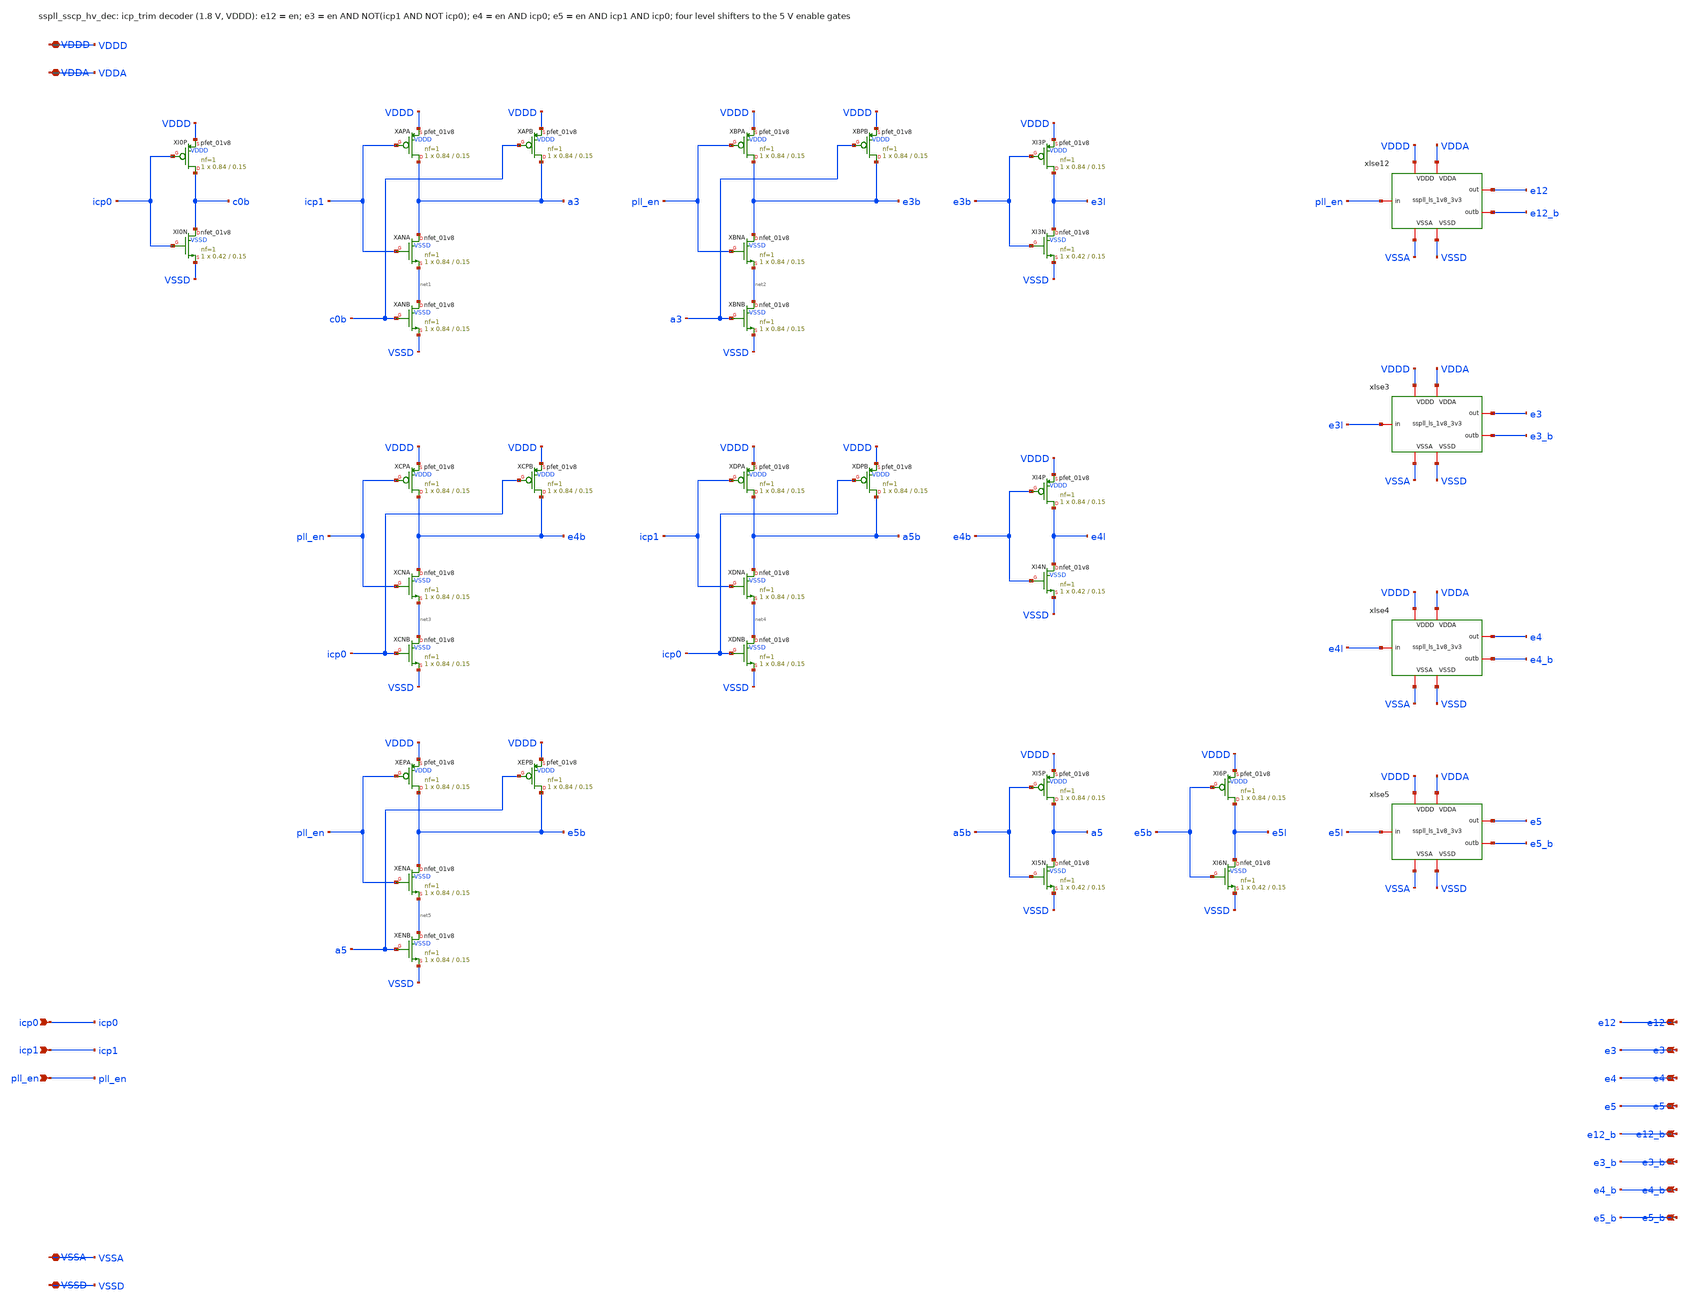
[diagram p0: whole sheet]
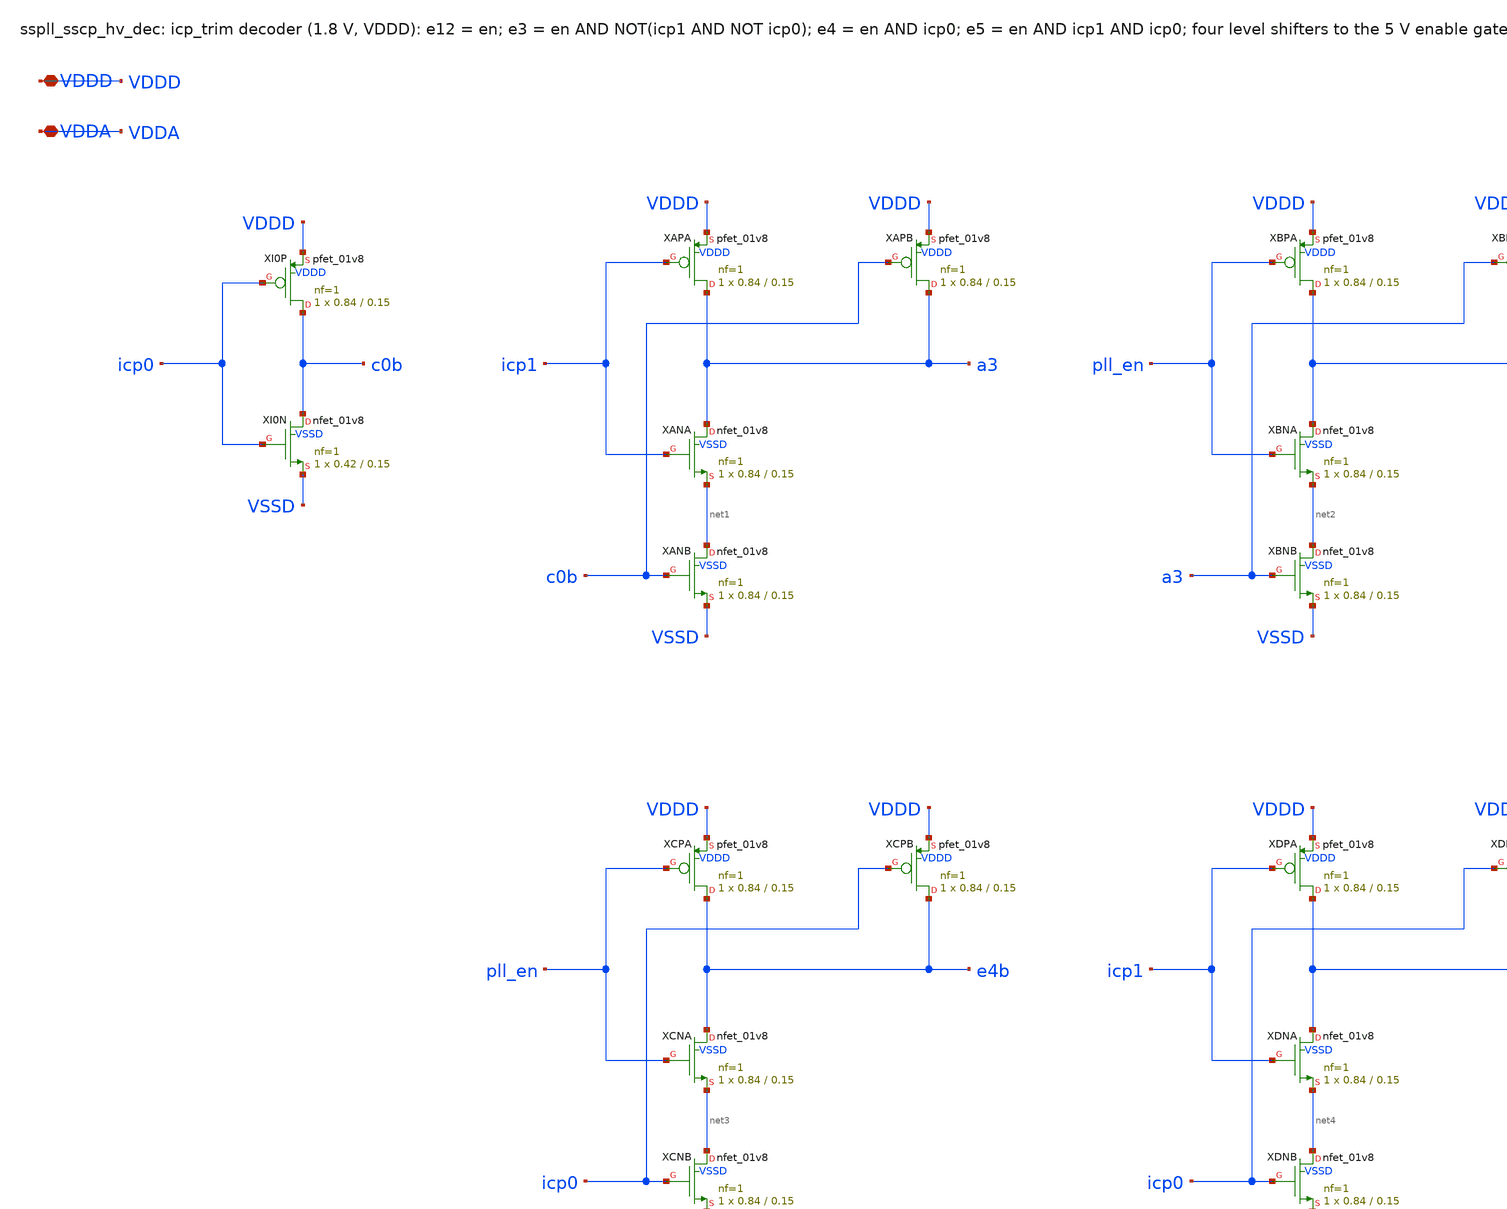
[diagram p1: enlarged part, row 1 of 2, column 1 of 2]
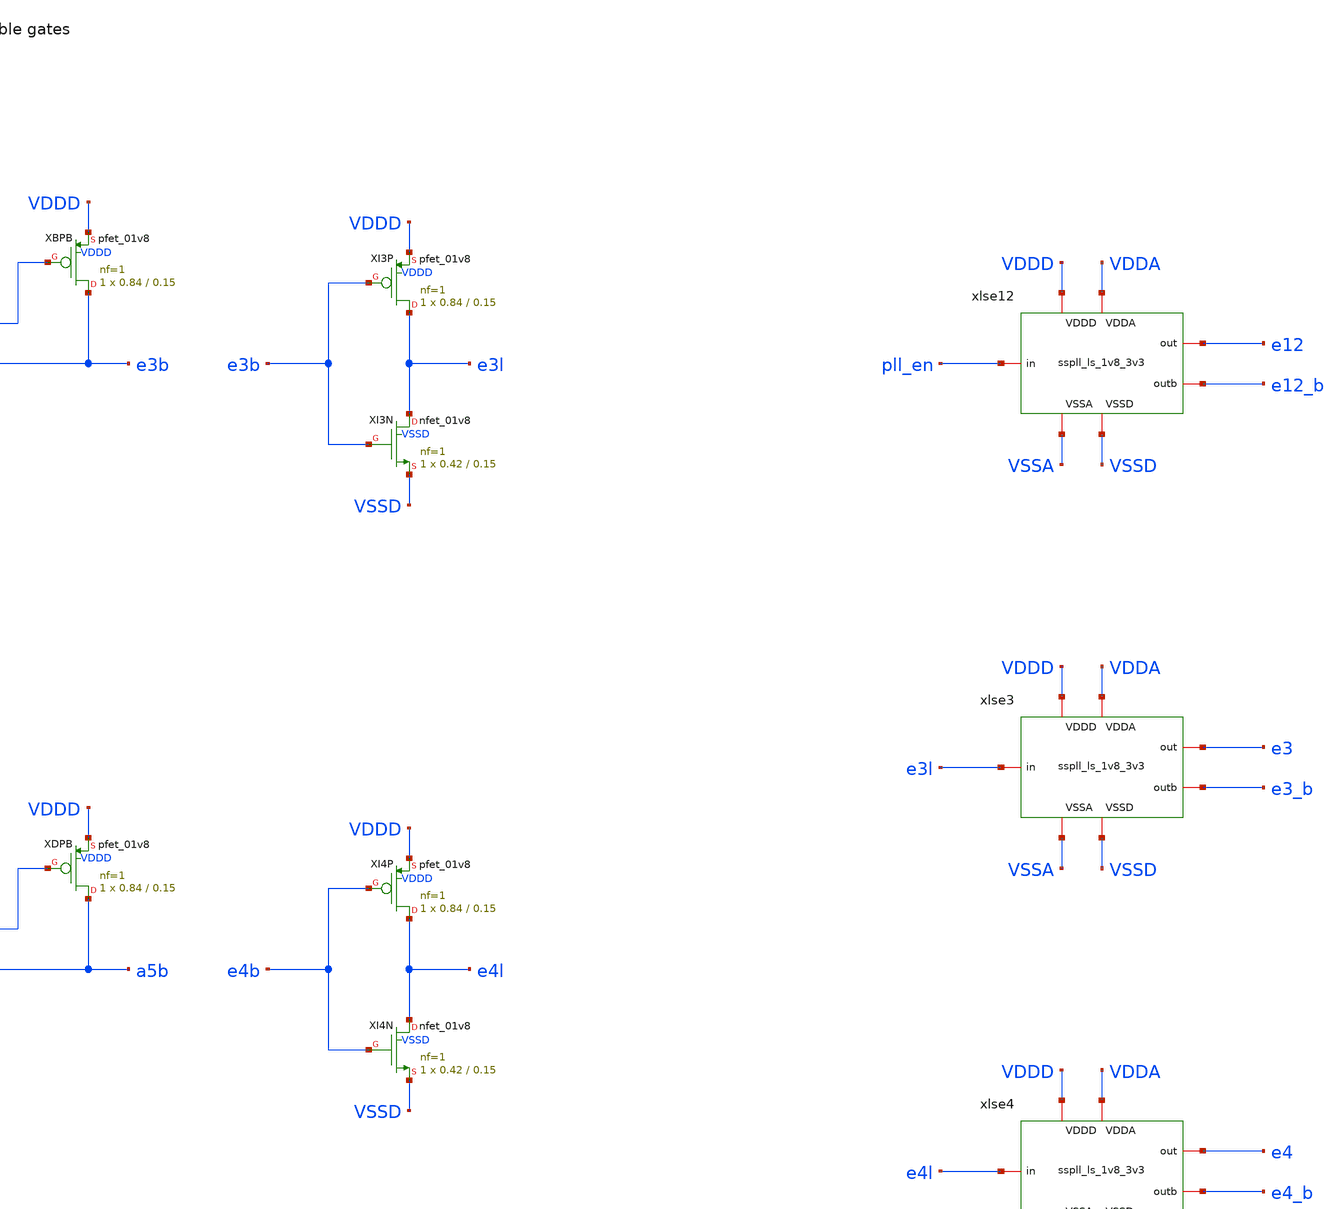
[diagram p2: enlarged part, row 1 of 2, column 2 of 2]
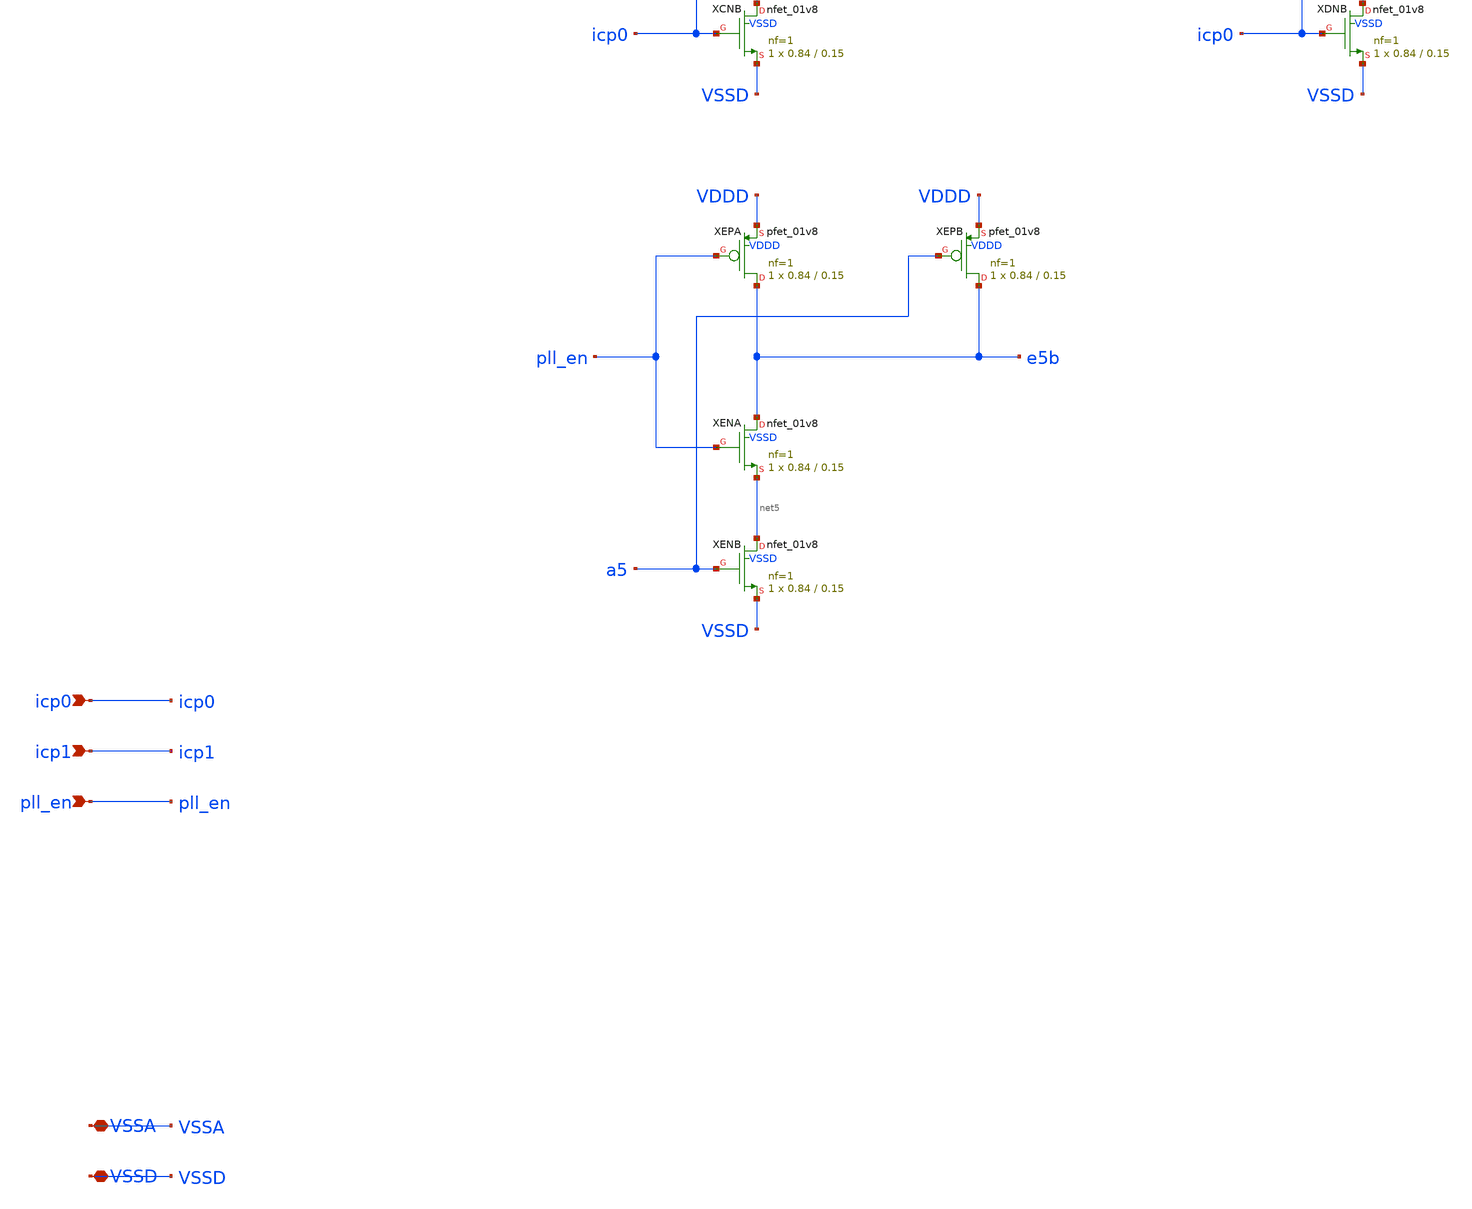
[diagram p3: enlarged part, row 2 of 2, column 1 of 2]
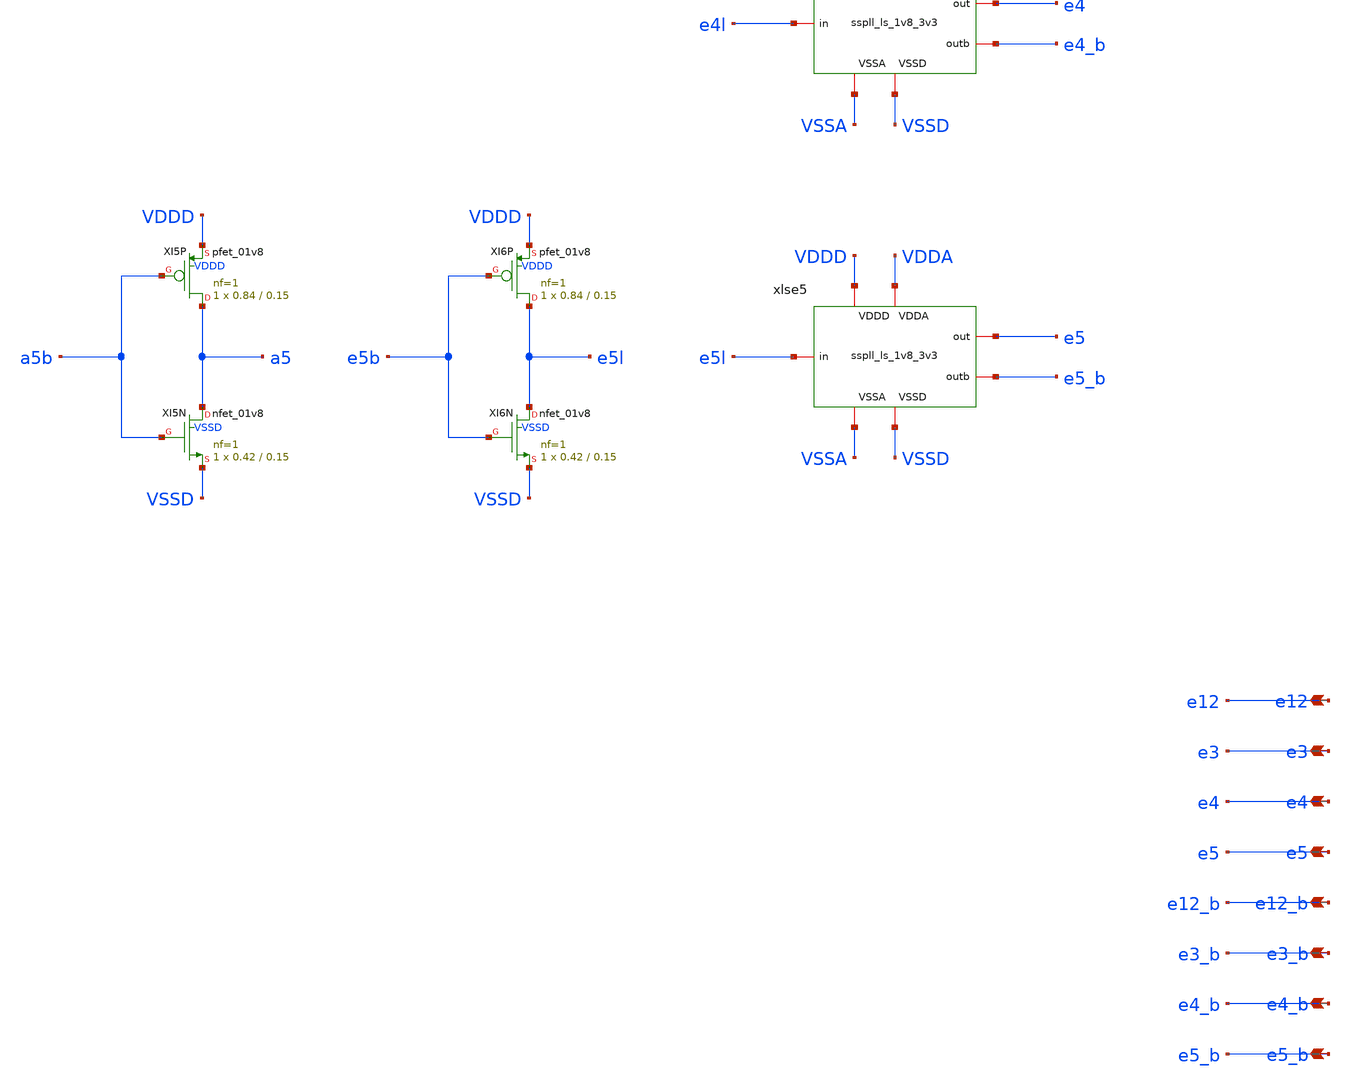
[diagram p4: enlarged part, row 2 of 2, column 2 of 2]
** sch_path: xschem/sscp_hv/sspll_sscp_hv_dec.sch
**.subckt sspll_sscp_hv_dec icp0 icp1 pll_en e12 e3 e4 e5 e12_b e3_b e4_b e5_b VDDD VDDA VSSA VSSD
*.ipin icp0
*.ipin icp1
*.ipin pll_en
*.opin e12
*.opin e3
*.opin e4
*.opin e5
*.opin e12_b
*.opin e3_b
*.opin e4_b
*.opin e5_b
*.iopin VDDD
*.iopin VDDA
*.iopin VSSA
*.iopin VSSD
XXI0P c0b icp0 VDDD VDDD sky130_fd_pr__pfet_01v8 L=0.15 W=0.84 nf=1 ad='int((nf+1)/2) * W/nf * 0.29'
+ as='int((nf+2)/2) * W/nf * 0.29' pd='2*int((nf+1)/2) * (W/nf + 0.29)' ps='2*int((nf+2)/2) * (W/nf + 0.29)'
+ nrd='0.29 / W' nrs='0.29 / W' sa=0 sb=0 sd=0 mult=1 m=1
XXI0N c0b icp0 VSSD VSSD sky130_fd_pr__nfet_01v8 L=0.15 W=0.42 nf=1 ad='int((nf+1)/2) * W/nf * 0.29'
+ as='int((nf+2)/2) * W/nf * 0.29' pd='2*int((nf+1)/2) * (W/nf + 0.29)' ps='2*int((nf+2)/2) * (W/nf + 0.29)'
+ nrd='0.29 / W' nrs='0.29 / W' sa=0 sb=0 sd=0 mult=1 m=1
XXAPA a3 icp1 VDDD VDDD sky130_fd_pr__pfet_01v8 L=0.15 W=0.84 nf=1 ad='int((nf+1)/2) * W/nf * 0.29' as='int((nf+2)/2) * W/nf * 0.29'
+ pd='2*int((nf+1)/2) * (W/nf + 0.29)' ps='2*int((nf+2)/2) * (W/nf + 0.29)' nrd='0.29 / W' nrs='0.29 / W'
+ sa=0 sb=0 sd=0 mult=1 m=1
XXAPB a3 c0b VDDD VDDD sky130_fd_pr__pfet_01v8 L=0.15 W=0.84 nf=1 ad='int((nf+1)/2) * W/nf * 0.29' as='int((nf+2)/2) * W/nf * 0.29'
+ pd='2*int((nf+1)/2) * (W/nf + 0.29)' ps='2*int((nf+2)/2) * (W/nf + 0.29)' nrd='0.29 / W' nrs='0.29 / W'
+ sa=0 sb=0 sd=0 mult=1 m=1
XXANA a3 icp1 net1 VSSD sky130_fd_pr__nfet_01v8 L=0.15 W=0.84 nf=1 ad='int((nf+1)/2) * W/nf * 0.29' as='int((nf+2)/2) * W/nf * 0.29'
+ pd='2*int((nf+1)/2) * (W/nf + 0.29)' ps='2*int((nf+2)/2) * (W/nf + 0.29)' nrd='0.29 / W' nrs='0.29 / W'
+ sa=0 sb=0 sd=0 mult=1 m=1
XXANB net1 c0b VSSD VSSD sky130_fd_pr__nfet_01v8 L=0.15 W=0.84 nf=1 ad='int((nf+1)/2) * W/nf * 0.29'
+ as='int((nf+2)/2) * W/nf * 0.29' pd='2*int((nf+1)/2) * (W/nf + 0.29)' ps='2*int((nf+2)/2) * (W/nf + 0.29)'
+ nrd='0.29 / W' nrs='0.29 / W' sa=0 sb=0 sd=0 mult=1 m=1
XXBPA e3b pll_en VDDD VDDD sky130_fd_pr__pfet_01v8 L=0.15 W=0.84 nf=1 ad='int((nf+1)/2) * W/nf * 0.29'
+ as='int((nf+2)/2) * W/nf * 0.29' pd='2*int((nf+1)/2) * (W/nf + 0.29)' ps='2*int((nf+2)/2) * (W/nf + 0.29)'
+ nrd='0.29 / W' nrs='0.29 / W' sa=0 sb=0 sd=0 mult=1 m=1
XXBPB e3b a3 VDDD VDDD sky130_fd_pr__pfet_01v8 L=0.15 W=0.84 nf=1 ad='int((nf+1)/2) * W/nf * 0.29' as='int((nf+2)/2) * W/nf * 0.29'
+ pd='2*int((nf+1)/2) * (W/nf + 0.29)' ps='2*int((nf+2)/2) * (W/nf + 0.29)' nrd='0.29 / W' nrs='0.29 / W'
+ sa=0 sb=0 sd=0 mult=1 m=1
XXBNA e3b pll_en net2 VSSD sky130_fd_pr__nfet_01v8 L=0.15 W=0.84 nf=1 ad='int((nf+1)/2) * W/nf * 0.29'
+ as='int((nf+2)/2) * W/nf * 0.29' pd='2*int((nf+1)/2) * (W/nf + 0.29)' ps='2*int((nf+2)/2) * (W/nf + 0.29)'
+ nrd='0.29 / W' nrs='0.29 / W' sa=0 sb=0 sd=0 mult=1 m=1
XXBNB net2 a3 VSSD VSSD sky130_fd_pr__nfet_01v8 L=0.15 W=0.84 nf=1 ad='int((nf+1)/2) * W/nf * 0.29' as='int((nf+2)/2) * W/nf * 0.29'
+ pd='2*int((nf+1)/2) * (W/nf + 0.29)' ps='2*int((nf+2)/2) * (W/nf + 0.29)' nrd='0.29 / W' nrs='0.29 / W'
+ sa=0 sb=0 sd=0 mult=1 m=1
XXCPA e4b pll_en VDDD VDDD sky130_fd_pr__pfet_01v8 L=0.15 W=0.84 nf=1 ad='int((nf+1)/2) * W/nf * 0.29'
+ as='int((nf+2)/2) * W/nf * 0.29' pd='2*int((nf+1)/2) * (W/nf + 0.29)' ps='2*int((nf+2)/2) * (W/nf + 0.29)'
+ nrd='0.29 / W' nrs='0.29 / W' sa=0 sb=0 sd=0 mult=1 m=1
XXCPB e4b icp0 VDDD VDDD sky130_fd_pr__pfet_01v8 L=0.15 W=0.84 nf=1 ad='int((nf+1)/2) * W/nf * 0.29'
+ as='int((nf+2)/2) * W/nf * 0.29' pd='2*int((nf+1)/2) * (W/nf + 0.29)' ps='2*int((nf+2)/2) * (W/nf + 0.29)'
+ nrd='0.29 / W' nrs='0.29 / W' sa=0 sb=0 sd=0 mult=1 m=1
XXCNA e4b pll_en net3 VSSD sky130_fd_pr__nfet_01v8 L=0.15 W=0.84 nf=1 ad='int((nf+1)/2) * W/nf * 0.29'
+ as='int((nf+2)/2) * W/nf * 0.29' pd='2*int((nf+1)/2) * (W/nf + 0.29)' ps='2*int((nf+2)/2) * (W/nf + 0.29)'
+ nrd='0.29 / W' nrs='0.29 / W' sa=0 sb=0 sd=0 mult=1 m=1
XXCNB net3 icp0 VSSD VSSD sky130_fd_pr__nfet_01v8 L=0.15 W=0.84 nf=1 ad='int((nf+1)/2) * W/nf * 0.29'
+ as='int((nf+2)/2) * W/nf * 0.29' pd='2*int((nf+1)/2) * (W/nf + 0.29)' ps='2*int((nf+2)/2) * (W/nf + 0.29)'
+ nrd='0.29 / W' nrs='0.29 / W' sa=0 sb=0 sd=0 mult=1 m=1
XXDPA a5b icp1 VDDD VDDD sky130_fd_pr__pfet_01v8 L=0.15 W=0.84 nf=1 ad='int((nf+1)/2) * W/nf * 0.29'
+ as='int((nf+2)/2) * W/nf * 0.29' pd='2*int((nf+1)/2) * (W/nf + 0.29)' ps='2*int((nf+2)/2) * (W/nf + 0.29)'
+ nrd='0.29 / W' nrs='0.29 / W' sa=0 sb=0 sd=0 mult=1 m=1
XXDPB a5b icp0 VDDD VDDD sky130_fd_pr__pfet_01v8 L=0.15 W=0.84 nf=1 ad='int((nf+1)/2) * W/nf * 0.29'
+ as='int((nf+2)/2) * W/nf * 0.29' pd='2*int((nf+1)/2) * (W/nf + 0.29)' ps='2*int((nf+2)/2) * (W/nf + 0.29)'
+ nrd='0.29 / W' nrs='0.29 / W' sa=0 sb=0 sd=0 mult=1 m=1
XXDNA a5b icp1 net4 VSSD sky130_fd_pr__nfet_01v8 L=0.15 W=0.84 nf=1 ad='int((nf+1)/2) * W/nf * 0.29'
+ as='int((nf+2)/2) * W/nf * 0.29' pd='2*int((nf+1)/2) * (W/nf + 0.29)' ps='2*int((nf+2)/2) * (W/nf + 0.29)'
+ nrd='0.29 / W' nrs='0.29 / W' sa=0 sb=0 sd=0 mult=1 m=1
XXDNB net4 icp0 VSSD VSSD sky130_fd_pr__nfet_01v8 L=0.15 W=0.84 nf=1 ad='int((nf+1)/2) * W/nf * 0.29'
+ as='int((nf+2)/2) * W/nf * 0.29' pd='2*int((nf+1)/2) * (W/nf + 0.29)' ps='2*int((nf+2)/2) * (W/nf + 0.29)'
+ nrd='0.29 / W' nrs='0.29 / W' sa=0 sb=0 sd=0 mult=1 m=1
XXEPA e5b pll_en VDDD VDDD sky130_fd_pr__pfet_01v8 L=0.15 W=0.84 nf=1 ad='int((nf+1)/2) * W/nf * 0.29'
+ as='int((nf+2)/2) * W/nf * 0.29' pd='2*int((nf+1)/2) * (W/nf + 0.29)' ps='2*int((nf+2)/2) * (W/nf + 0.29)'
+ nrd='0.29 / W' nrs='0.29 / W' sa=0 sb=0 sd=0 mult=1 m=1
XXEPB e5b a5 VDDD VDDD sky130_fd_pr__pfet_01v8 L=0.15 W=0.84 nf=1 ad='int((nf+1)/2) * W/nf * 0.29' as='int((nf+2)/2) * W/nf * 0.29'
+ pd='2*int((nf+1)/2) * (W/nf + 0.29)' ps='2*int((nf+2)/2) * (W/nf + 0.29)' nrd='0.29 / W' nrs='0.29 / W'
+ sa=0 sb=0 sd=0 mult=1 m=1
XXENA e5b pll_en net5 VSSD sky130_fd_pr__nfet_01v8 L=0.15 W=0.84 nf=1 ad='int((nf+1)/2) * W/nf * 0.29'
+ as='int((nf+2)/2) * W/nf * 0.29' pd='2*int((nf+1)/2) * (W/nf + 0.29)' ps='2*int((nf+2)/2) * (W/nf + 0.29)'
+ nrd='0.29 / W' nrs='0.29 / W' sa=0 sb=0 sd=0 mult=1 m=1
XXENB net5 a5 VSSD VSSD sky130_fd_pr__nfet_01v8 L=0.15 W=0.84 nf=1 ad='int((nf+1)/2) * W/nf * 0.29' as='int((nf+2)/2) * W/nf * 0.29'
+ pd='2*int((nf+1)/2) * (W/nf + 0.29)' ps='2*int((nf+2)/2) * (W/nf + 0.29)' nrd='0.29 / W' nrs='0.29 / W'
+ sa=0 sb=0 sd=0 mult=1 m=1
XXI3P e3l e3b VDDD VDDD sky130_fd_pr__pfet_01v8 L=0.15 W=0.84 nf=1 ad='int((nf+1)/2) * W/nf * 0.29' as='int((nf+2)/2) * W/nf * 0.29'
+ pd='2*int((nf+1)/2) * (W/nf + 0.29)' ps='2*int((nf+2)/2) * (W/nf + 0.29)' nrd='0.29 / W' nrs='0.29 / W'
+ sa=0 sb=0 sd=0 mult=1 m=1
XXI3N e3l e3b VSSD VSSD sky130_fd_pr__nfet_01v8 L=0.15 W=0.42 nf=1 ad='int((nf+1)/2) * W/nf * 0.29' as='int((nf+2)/2) * W/nf * 0.29'
+ pd='2*int((nf+1)/2) * (W/nf + 0.29)' ps='2*int((nf+2)/2) * (W/nf + 0.29)' nrd='0.29 / W' nrs='0.29 / W'
+ sa=0 sb=0 sd=0 mult=1 m=1
XXI4P e4l e4b VDDD VDDD sky130_fd_pr__pfet_01v8 L=0.15 W=0.84 nf=1 ad='int((nf+1)/2) * W/nf * 0.29' as='int((nf+2)/2) * W/nf * 0.29'
+ pd='2*int((nf+1)/2) * (W/nf + 0.29)' ps='2*int((nf+2)/2) * (W/nf + 0.29)' nrd='0.29 / W' nrs='0.29 / W'
+ sa=0 sb=0 sd=0 mult=1 m=1
XXI4N e4l e4b VSSD VSSD sky130_fd_pr__nfet_01v8 L=0.15 W=0.42 nf=1 ad='int((nf+1)/2) * W/nf * 0.29' as='int((nf+2)/2) * W/nf * 0.29'
+ pd='2*int((nf+1)/2) * (W/nf + 0.29)' ps='2*int((nf+2)/2) * (W/nf + 0.29)' nrd='0.29 / W' nrs='0.29 / W'
+ sa=0 sb=0 sd=0 mult=1 m=1
XXI5P a5 a5b VDDD VDDD sky130_fd_pr__pfet_01v8 L=0.15 W=0.84 nf=1 ad='int((nf+1)/2) * W/nf * 0.29' as='int((nf+2)/2) * W/nf * 0.29'
+ pd='2*int((nf+1)/2) * (W/nf + 0.29)' ps='2*int((nf+2)/2) * (W/nf + 0.29)' nrd='0.29 / W' nrs='0.29 / W'
+ sa=0 sb=0 sd=0 mult=1 m=1
XXI5N a5 a5b VSSD VSSD sky130_fd_pr__nfet_01v8 L=0.15 W=0.42 nf=1 ad='int((nf+1)/2) * W/nf * 0.29' as='int((nf+2)/2) * W/nf * 0.29'
+ pd='2*int((nf+1)/2) * (W/nf + 0.29)' ps='2*int((nf+2)/2) * (W/nf + 0.29)' nrd='0.29 / W' nrs='0.29 / W'
+ sa=0 sb=0 sd=0 mult=1 m=1
XXI6P e5l e5b VDDD VDDD sky130_fd_pr__pfet_01v8 L=0.15 W=0.84 nf=1 ad='int((nf+1)/2) * W/nf * 0.29' as='int((nf+2)/2) * W/nf * 0.29'
+ pd='2*int((nf+1)/2) * (W/nf + 0.29)' ps='2*int((nf+2)/2) * (W/nf + 0.29)' nrd='0.29 / W' nrs='0.29 / W'
+ sa=0 sb=0 sd=0 mult=1 m=1
XXI6N e5l e5b VSSD VSSD sky130_fd_pr__nfet_01v8 L=0.15 W=0.42 nf=1 ad='int((nf+1)/2) * W/nf * 0.29' as='int((nf+2)/2) * W/nf * 0.29'
+ pd='2*int((nf+1)/2) * (W/nf + 0.29)' ps='2*int((nf+2)/2) * (W/nf + 0.29)' nrd='0.29 / W' nrs='0.29 / W'
+ sa=0 sb=0 sd=0 mult=1 m=1
xlse12 pll_en e12 e12_b VDDD VDDA VSSA VSSD sspll_ls_1v8_3v3
xlse3 e3l e3 e3_b VDDD VDDA VSSA VSSD sspll_ls_1v8_3v3
xlse4 e4l e4 e4_b VDDD VDDA VSSA VSSD sspll_ls_1v8_3v3
xlse5 e5l e5 e5_b VDDD VDDA VSSA VSSD sspll_ls_1v8_3v3
**.ends

* expanding   symbol:  ../cco_hv/sspll_ls_1v8_3v3.sym # of pins=7
** sym_path: xschem/cco_hv/sspll_ls_1v8_3v3.sym
** sch_path: xschem/cco_hv/sspll_ls_1v8_3v3.sch
.subckt sspll_ls_1v8_3v3 in out outb VDDD VDDA VSSA VSSD
*.iopin VDDD
*.iopin VDDA
*.iopin VSSD
*.iopin VSSA
*.ipin in
*.opin outb
*.opin out
XXPI net1 in VDDD VDDD sky130_fd_pr__pfet_01v8 L=0.15 W=1 nf=1 ad='int((nf+1)/2) * W/nf * 0.29' as='int((nf+2)/2) * W/nf * 0.29'
+ pd='2*int((nf+1)/2) * (W/nf + 0.29)' ps='2*int((nf+2)/2) * (W/nf + 0.29)' nrd='0.29 / W' nrs='0.29 / W'
+ sa=0 sb=0 sd=0 mult=1 m=1
XXNI net1 in VSSD VSSD sky130_fd_pr__nfet_01v8 L=0.15 W=0.5 nf=1 ad='int((nf+1)/2) * W/nf * 0.29' as='int((nf+2)/2) * W/nf * 0.29'
+ pd='2*int((nf+1)/2) * (W/nf + 0.29)' ps='2*int((nf+2)/2) * (W/nf + 0.29)' nrd='0.29 / W' nrs='0.29 / W'
+ sa=0 sb=0 sd=0 mult=1 m=1
XXP1 net2 net3 VDDA VDDA sky130_fd_pr__pfet_g5v0d10v5 L=0.5 W=1 nf=1 ad='int((nf+1)/2) * W/nf * 0.29'
+ as='int((nf+2)/2) * W/nf * 0.29' pd='2*int((nf+1)/2) * (W/nf + 0.29)' ps='2*int((nf+2)/2) * (W/nf + 0.29)'
+ nrd='0.29 / W' nrs='0.29 / W' sa=0 sb=0 sd=0 mult=1 m=1
XXP2 net3 net2 VDDA VDDA sky130_fd_pr__pfet_g5v0d10v5 L=0.5 W=1 nf=1 ad='int((nf+1)/2) * W/nf * 0.29'
+ as='int((nf+2)/2) * W/nf * 0.29' pd='2*int((nf+1)/2) * (W/nf + 0.29)' ps='2*int((nf+2)/2) * (W/nf + 0.29)'
+ nrd='0.29 / W' nrs='0.29 / W' sa=0 sb=0 sd=0 mult=1 m=1
XXN1 net2 in VSSA VSSA sky130_fd_pr__nfet_g5v0d10v5 L=0.5 W=3 nf=1 ad='int((nf+1)/2) * W/nf * 0.29' as='int((nf+2)/2) * W/nf * 0.29'
+ pd='2*int((nf+1)/2) * (W/nf + 0.29)' ps='2*int((nf+2)/2) * (W/nf + 0.29)' nrd='0.29 / W' nrs='0.29 / W'
+ sa=0 sb=0 sd=0 mult=1 m=1
XXN2 net3 net1 VSSA VSSA sky130_fd_pr__nfet_g5v0d10v5 L=0.5 W=3 nf=1 ad='int((nf+1)/2) * W/nf * 0.29'
+ as='int((nf+2)/2) * W/nf * 0.29' pd='2*int((nf+1)/2) * (W/nf + 0.29)' ps='2*int((nf+2)/2) * (W/nf + 0.29)'
+ nrd='0.29 / W' nrs='0.29 / W' sa=0 sb=0 sd=0 mult=1 m=1
XXPB outb net3 VDDA VDDA sky130_fd_pr__pfet_g5v0d10v5 L=0.5 W=2 nf=1 ad='int((nf+1)/2) * W/nf * 0.29'
+ as='int((nf+2)/2) * W/nf * 0.29' pd='2*int((nf+1)/2) * (W/nf + 0.29)' ps='2*int((nf+2)/2) * (W/nf + 0.29)'
+ nrd='0.29 / W' nrs='0.29 / W' sa=0 sb=0 sd=0 mult=1 m=1
XXNB outb net3 VSSA VSSA sky130_fd_pr__nfet_g5v0d10v5 L=0.5 W=1 nf=1 ad='int((nf+1)/2) * W/nf * 0.29'
+ as='int((nf+2)/2) * W/nf * 0.29' pd='2*int((nf+1)/2) * (W/nf + 0.29)' ps='2*int((nf+2)/2) * (W/nf + 0.29)'
+ nrd='0.29 / W' nrs='0.29 / W' sa=0 sb=0 sd=0 mult=1 m=1
XXPO out net2 VDDA VDDA sky130_fd_pr__pfet_g5v0d10v5 L=0.5 W=2 nf=1 ad='int((nf+1)/2) * W/nf * 0.29'
+ as='int((nf+2)/2) * W/nf * 0.29' pd='2*int((nf+1)/2) * (W/nf + 0.29)' ps='2*int((nf+2)/2) * (W/nf + 0.29)'
+ nrd='0.29 / W' nrs='0.29 / W' sa=0 sb=0 sd=0 mult=1 m=1
XXNO out net2 VSSA VSSA sky130_fd_pr__nfet_g5v0d10v5 L=0.5 W=1 nf=1 ad='int((nf+1)/2) * W/nf * 0.29'
+ as='int((nf+2)/2) * W/nf * 0.29' pd='2*int((nf+1)/2) * (W/nf + 0.29)' ps='2*int((nf+2)/2) * (W/nf + 0.29)'
+ nrd='0.29 / W' nrs='0.29 / W' sa=0 sb=0 sd=0 mult=1 m=1
.ends

.end
